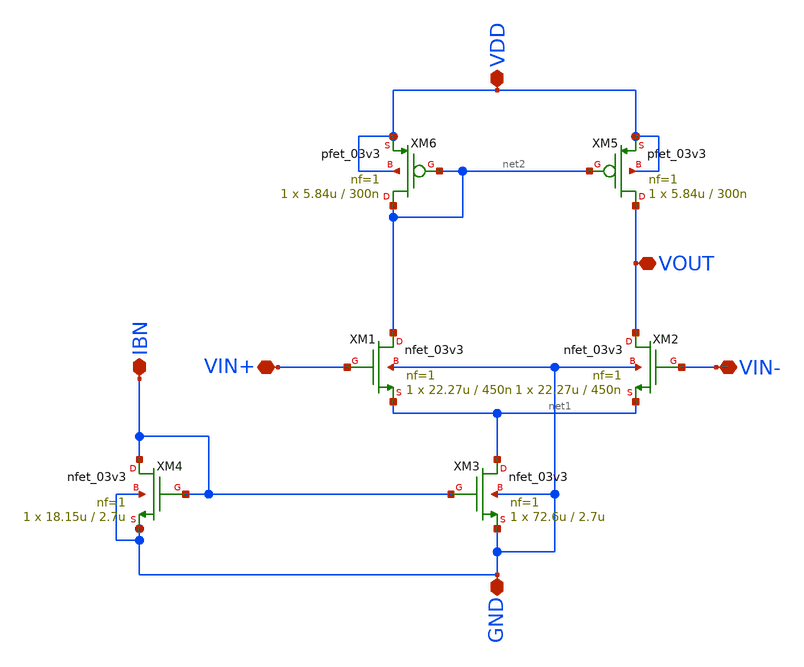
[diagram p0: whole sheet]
** sch_path: OTA_5T.sch
**.subckt OTA_5T VDD GND VIN- VIN+ VOUT IBN
*.iopin VDD
*.iopin GND
*.iopin VIN-
*.iopin VIN+
*.iopin VOUT
*.iopin IBN
XM1 net2 VIN+ net1 GND nfet_03v3 L=450n W=22.27u nf=1 ad='int((nf+1)/2) * W/nf * 0.18u' as='int((nf+2)/2) * W/nf * 0.18u'
+ pd='2*int((nf+1)/2) * (W/nf + 0.18u)' ps='2*int((nf+2)/2) * (W/nf + 0.18u)' nrd='0.18u / W' nrs='0.18u / W'
+ sa=0 sb=0 sd=0 m=1
XM2 VOUT VIN- net1 GND nfet_03v3 L=450n W=22.27u nf=1 ad='int((nf+1)/2) * W/nf * 0.18u' as='int((nf+2)/2) * W/nf * 0.18u'
+ pd='2*int((nf+1)/2) * (W/nf + 0.18u)' ps='2*int((nf+2)/2) * (W/nf + 0.18u)' nrd='0.18u / W' nrs='0.18u / W'
+ sa=0 sb=0 sd=0 m=1
XM4 IBN IBN GND GND nfet_03v3 L=2.7u W=18.15u nf=1 ad='int((nf+1)/2) * W/nf * 0.18u' as='int((nf+2)/2) * W/nf * 0.18u'
+ pd='2*int((nf+1)/2) * (W/nf + 0.18u)' ps='2*int((nf+2)/2) * (W/nf + 0.18u)' nrd='0.18u / W' nrs='0.18u / W'
+ sa=0 sb=0 sd=0 m=1
XM5 VOUT net2 VDD VDD pfet_03v3 L=300n W=5.84u nf=1 ad='int((nf+1)/2) * W/nf * 0.18u' as='int((nf+2)/2) * W/nf * 0.18u'
+ pd='2*int((nf+1)/2) * (W/nf + 0.18u)' ps='2*int((nf+2)/2) * (W/nf + 0.18u)' nrd='0.18u / W' nrs='0.18u / W'
+ sa=0 sb=0 sd=0 m=1
XM6 net2 net2 VDD VDD pfet_03v3 L=300n W=5.84u nf=1 ad='int((nf+1)/2) * W/nf * 0.18u' as='int((nf+2)/2) * W/nf * 0.18u'
+ pd='2*int((nf+1)/2) * (W/nf + 0.18u)' ps='2*int((nf+2)/2) * (W/nf + 0.18u)' nrd='0.18u / W' nrs='0.18u / W'
+ sa=0 sb=0 sd=0 m=1
XM3 net1 IBN GND GND nfet_03v3 L=2.7u W=72.6u nf=1 ad='int((nf+1)/2) * W/nf * 0.18u' as='int((nf+2)/2) * W/nf * 0.18u'
+ pd='2*int((nf+1)/2) * (W/nf + 0.18u)' ps='2*int((nf+2)/2) * (W/nf + 0.18u)' nrd='0.18u / W' nrs='0.18u / W'
+ sa=0 sb=0 sd=0 m=1
**.ends
.end
